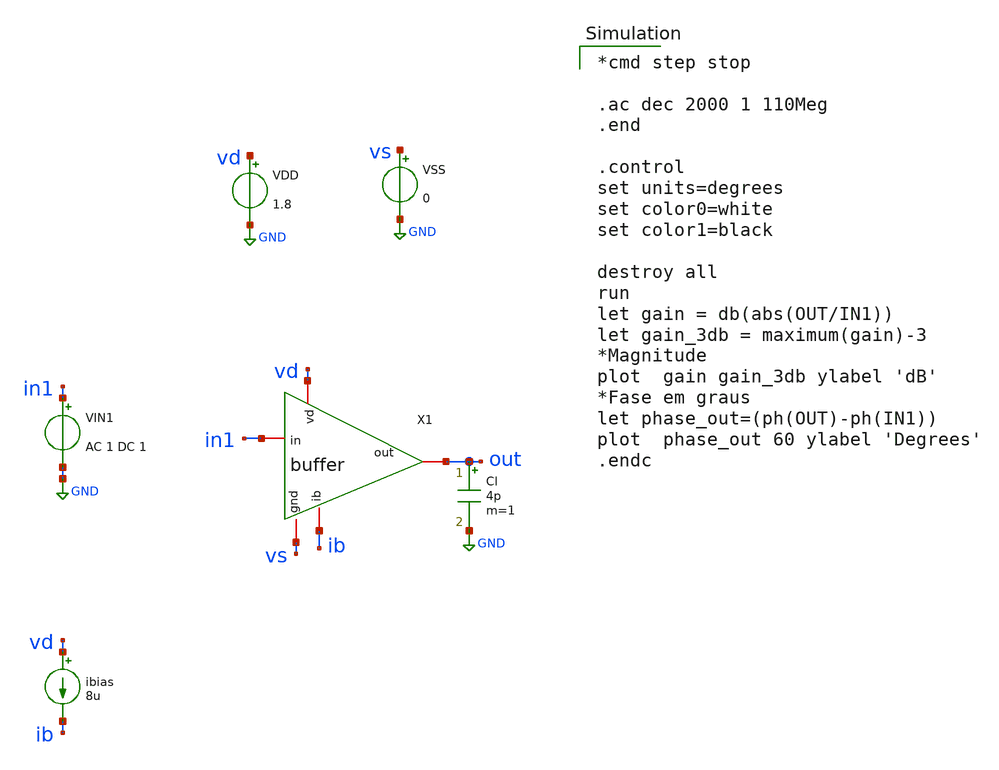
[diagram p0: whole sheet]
** sch_path: buffer/xschem/buffer_tb-ac.sch
* Copyright 2020 Stefan Frederik Schippers
* Licensed under the Apache License, Version 2.0 (the "License");
* you may not use this file except in compliance with the License.
* You may obtain a copy of the License at
* https://www.apache.org/licenses/LICENSE-2.0
* Unless required by applicable law or agreed to in writing, software
* distributed under the License is distributed on an "AS IS" BASIS,
* WITHOUT WARRANTIES OR CONDITIONS OF ANY KIND, either express or implied.
* See the License for the specific language governing permissions and
* limitations under the License.
**.subckt buffer_tb-ac
VIN1 in1 GND AC 1 DC 1
ibias vd ib 8u
VDD vd GND 1.8
VSS vs GND 0
X1 vd in1 out ib vs buffer
Cl out GND 4p m=1
**** begin user architecture code

*cmd step stop

.ac dec 2000 1 110Meg
.end

.control
set units=degrees
set color0=white
set color1=black

destroy all
run
let gain = db(abs(OUT/IN1))
let gain_3db = maximum(gain)-3
*Magnitude
plot  gain gain_3db ylabel 'dB'
*Fase em graus
let phase_out=(ph(OUT)-ph(IN1))
plot  phase_out 60 ylabel 'Degrees'
.endc

 .lib $::SKYWATER_MODELS/sky130.lib.spice tt
.include $::SKYWATER_STDCELLS/sky130_fd_sc_hd.spice

**** end user architecture code
**.ends

* expanding   symbol:  /home/hugodg/projects-sky130/temp-sensor/buffer/xschem/buffer.sym # of pins=5
** sym_path: buffer/xschem/buffer.sym
** sch_path: buffer/xschem/buffer.sch
.subckt buffer vd in out ib gnd
*.iopin vd
*.iopin ib
*.iopin out
*.iopin in
*.iopin gnd
**** begin user architecture code




**** end user architecture code
XM3 net2 net2 vd vd sky130_fd_pr__pfet_01v8 L=1 W=1 nf=1 ad='int((nf+1)/2) * W/nf * 0.29' as='int((nf+2)/2) * W/nf * 0.29'
+ pd='2*int((nf+1)/2) * (W/nf + 0.29)' ps='2*int((nf+2)/2) * (W/nf + 0.29)' nrd='0.29 / W' nrs='0.29 / W'
+ sa=0 sb=0 sd=0 mult=1 m=1
XM1 net2 out net3 net3 sky130_fd_pr__nfet_01v8 L=1 W=10 nf=1 ad='int((nf+1)/2) * W/nf * 0.29' as='int((nf+2)/2) * W/nf * 0.29'
+ pd='2*int((nf+1)/2) * (W/nf + 0.29)' ps='2*int((nf+2)/2) * (W/nf + 0.29)' nrd='0.29 / W' nrs='0.29 / W'
+ sa=0 sb=0 sd=0 mult=1 m=1
XM2 net4 in net3 net3 sky130_fd_pr__nfet_01v8 L=1 W=10 nf=1 ad='int((nf+1)/2) * W/nf * 0.29' as='int((nf+2)/2) * W/nf * 0.29'
+ pd='2*int((nf+1)/2) * (W/nf + 0.29)' ps='2*int((nf+2)/2) * (W/nf + 0.29)' nrd='0.29 / W' nrs='0.29 / W'
+ sa=0 sb=0 sd=0 mult=1 m=1
XM4 net4 net4 vd vd sky130_fd_pr__pfet_01v8 L=1 W=1 nf=1 ad='int((nf+1)/2) * W/nf * 0.29' as='int((nf+2)/2) * W/nf * 0.29'
+ pd='2*int((nf+1)/2) * (W/nf + 0.29)' ps='2*int((nf+2)/2) * (W/nf + 0.29)' nrd='0.29 / W' nrs='0.29 / W'
+ sa=0 sb=0 sd=0 mult=1 m=1
XM5 net3 ib gnd gnd sky130_fd_pr__nfet_01v8 L=1 W=1 nf=1 ad='int((nf+1)/2) * W/nf * 0.29' as='int((nf+2)/2) * W/nf * 0.29'
+ pd='2*int((nf+1)/2) * (W/nf + 0.29)' ps='2*int((nf+2)/2) * (W/nf + 0.29)' nrd='0.29 / W' nrs='0.29 / W'
+ sa=0 sb=0 sd=0 mult=1 m=1
XM6 out net4 vd vd sky130_fd_pr__pfet_01v8 L=1 W=10 nf=1 ad='int((nf+1)/2) * W/nf * 0.29' as='int((nf+2)/2) * W/nf * 0.29'
+ pd='2*int((nf+1)/2) * (W/nf + 0.29)' ps='2*int((nf+2)/2) * (W/nf + 0.29)' nrd='0.29 / W' nrs='0.29 / W'
+ sa=0 sb=0 sd=0 mult=1 m=1
XM7 out net1 gnd gnd sky130_fd_pr__nfet_01v8 L=1 W=10 nf=1 ad='int((nf+1)/2) * W/nf * 0.29' as='int((nf+2)/2) * W/nf * 0.29'
+ pd='2*int((nf+1)/2) * (W/nf + 0.29)' ps='2*int((nf+2)/2) * (W/nf + 0.29)' nrd='0.29 / W' nrs='0.29 / W'
+ sa=0 sb=0 sd=0 mult=1 m=1
XM8 net1 net2 vd vd sky130_fd_pr__pfet_01v8 L=1 W=10 nf=1 ad='int((nf+1)/2) * W/nf * 0.29' as='int((nf+2)/2) * W/nf * 0.29'
+ pd='2*int((nf+1)/2) * (W/nf + 0.29)' ps='2*int((nf+2)/2) * (W/nf + 0.29)' nrd='0.29 / W' nrs='0.29 / W'
+ sa=0 sb=0 sd=0 mult=1 m=1
XM9 net1 net1 gnd gnd sky130_fd_pr__nfet_01v8 L=1 W=10 nf=1 ad='int((nf+1)/2) * W/nf * 0.29' as='int((nf+2)/2) * W/nf * 0.29'
+ pd='2*int((nf+1)/2) * (W/nf + 0.29)' ps='2*int((nf+2)/2) * (W/nf + 0.29)' nrd='0.29 / W' nrs='0.29 / W'
+ sa=0 sb=0 sd=0 mult=1 m=1
XM10 ib ib gnd gnd sky130_fd_pr__nfet_01v8 L=1 W=1 nf=1 ad='int((nf+1)/2) * W/nf * 0.29' as='int((nf+2)/2) * W/nf * 0.29'
+ pd='2*int((nf+1)/2) * (W/nf + 0.29)' ps='2*int((nf+2)/2) * (W/nf + 0.29)' nrd='0.29 / W' nrs='0.29 / W'
+ sa=0 sb=0 sd=0 mult=1 m=1
.ends

.GLOBAL GND
.end
